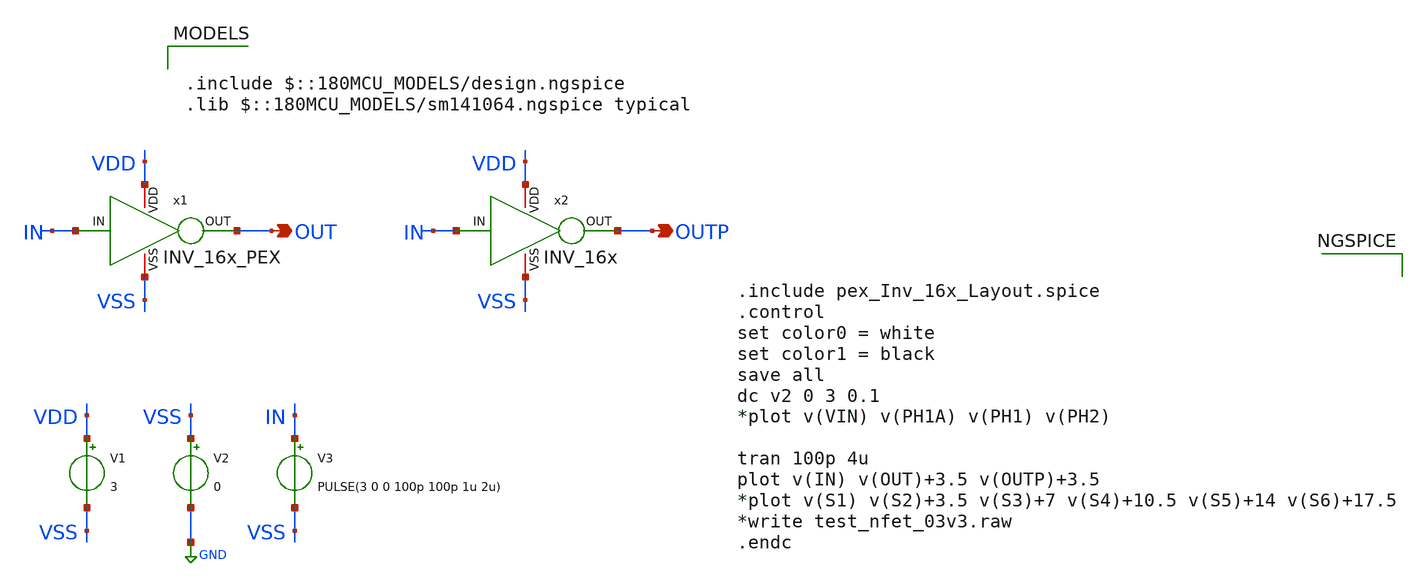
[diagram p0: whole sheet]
** sch_path: SCOP_INPUT_AND_MUX_PAKISTAN_03/Xschem/Logic_Gates/INV_16x_TB.sch
**.subckt INV_16x_TB OUT OUTP
*.opin OUT
*.opin OUTP
V1 VDD VSS 3
V2 VSS GND 0
V3 IN VSS PULSE(3 0 0 100p 100p 1u 2u)
x2 VDD OUTP IN VSS INV_16x
x1 VDD OUT IN VSS INV_16x_PEX
**** begin user architecture code

.include $::180MCU_MODELS/design.ngspice
.lib $::180MCU_MODELS/sm141064.ngspice typical



.include pex_Inv_16x_Layout.spice
.control
set color0 = white
set color1 = black
save all
dc v2 0 3 0.1
*plot v(VIN) v(PH1A) v(PH1) v(PH2)

tran 100p 4u
plot v(IN) v(OUT)+3.5 v(OUTP)+3.5
*plot v(S1) v(S2)+3.5 v(S3)+7 v(S4)+10.5 v(S5)+14 v(S6)+17.5
*write test_nfet_03v3.raw
.endc


**** end user architecture code
**.ends

* expanding   symbol:  INV_16x.sym # of pins=4
** sym_path: SCOP_INPUT_AND_MUX_PAKISTAN_03/Xschem/Logic_Gates/INV_16x.sym
** sch_path: SCOP_INPUT_AND_MUX_PAKISTAN_03/Xschem/Logic_Gates/INV_16x.sch
.subckt INV_16x VDD OUT IN VSS
*.iopin VDD
*.iopin VSS
*.ipin IN
*.opin OUT
XM1 OUT IN VSS VSS nfet_03v3 L=2.24u W=0.22u nf=1 ad='int((nf+1)/2) * W/nf * 0.18u' as='int((nf+2)/2) * W/nf * 0.18u'
+ pd='2*int((nf+1)/2) * (W/nf + 0.18u)' ps='2*int((nf+2)/2) * (W/nf + 0.18u)' nrd='0.18u / W' nrs='0.18u / W'
+ sa=0 sb=0 sd=0 m=1
XM2 OUT IN VDD VDD pfet_03v3 L=2.24u W=0.44u nf=1 ad='int((nf+1)/2) * W/nf * 0.18u' as='int((nf+2)/2) * W/nf * 0.18u'
+ pd='2*int((nf+1)/2) * (W/nf + 0.18u)' ps='2*int((nf+2)/2) * (W/nf + 0.18u)' nrd='0.18u / W' nrs='0.18u / W'
+ sa=0 sb=0 sd=0 m=1
.ends

.GLOBAL GND
.end
